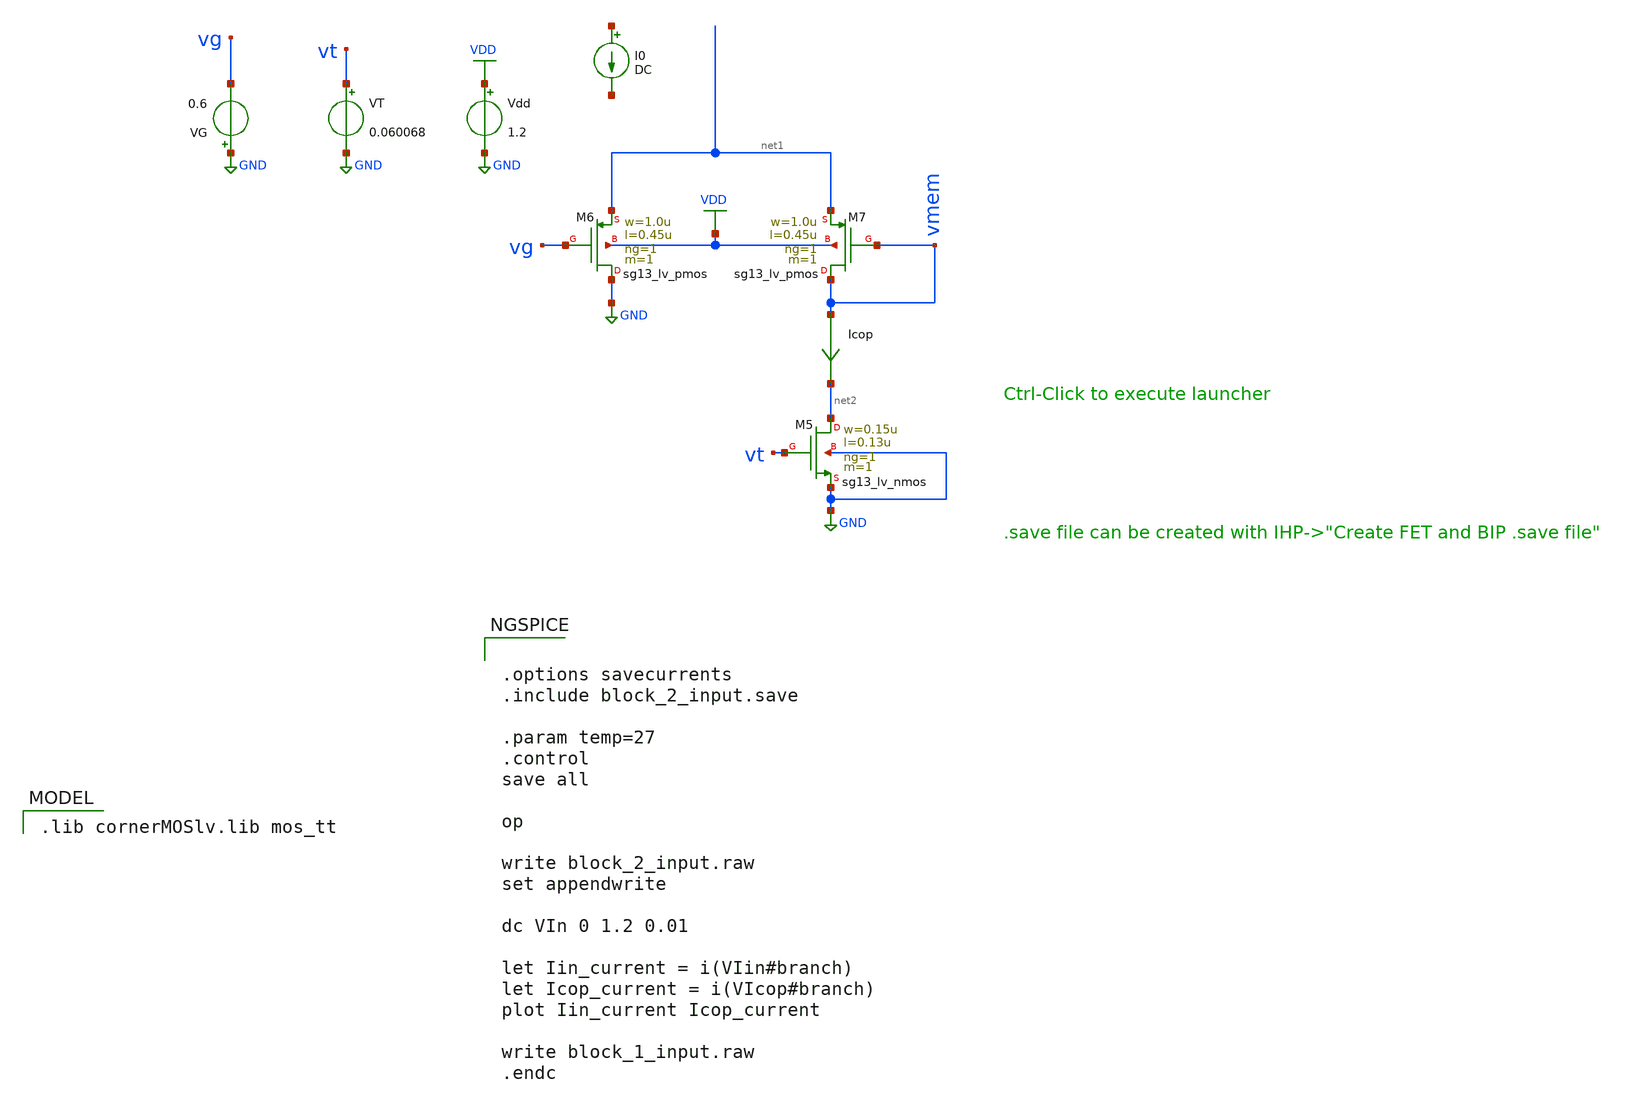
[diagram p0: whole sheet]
** sch_path: blocks/composite/dpi_adexp_neuron/design_data/xschem/block_2_input.sch
* Copyright 2023 IHP PDK Authors
**.subckt block_2_input
XM6 GND vg net1 VDD sg13_lv_pmos w=1.0u l=0.45u ng=1 m=1 mm_ok=1
XM7 vmem vmem net1 VDD sg13_lv_pmos w=1.0u l=0.45u ng=1 m=1 mm_ok=1
XM5 net2 vt GND GND sg13_lv_nmos w=0.15u l=0.13u ng=1 m=1 mm_ok=1
Vdd VDD GND 1.2
Icop vmem net2 0
.save i(icop)
VT vt GND 0.060068
VG GND vg 0.6
I0 net3 net4 DC
**** begin user architecture code


.options savecurrents
.include block_2_input.save

.param temp=27
.control
save all

op

write block_2_input.raw
set appendwrite

dc VIn 0 1.2 0.01

let Iin_current = i(VIin#branch)
let Icop_current = i(VIcop#branch)
plot Iin_current Icop_current

write block_1_input.raw
.endc


 .lib cornerMOSlv.lib mos_tt

**** end user architecture code
**.ends
.GLOBAL VDD
.GLOBAL GND
.end
